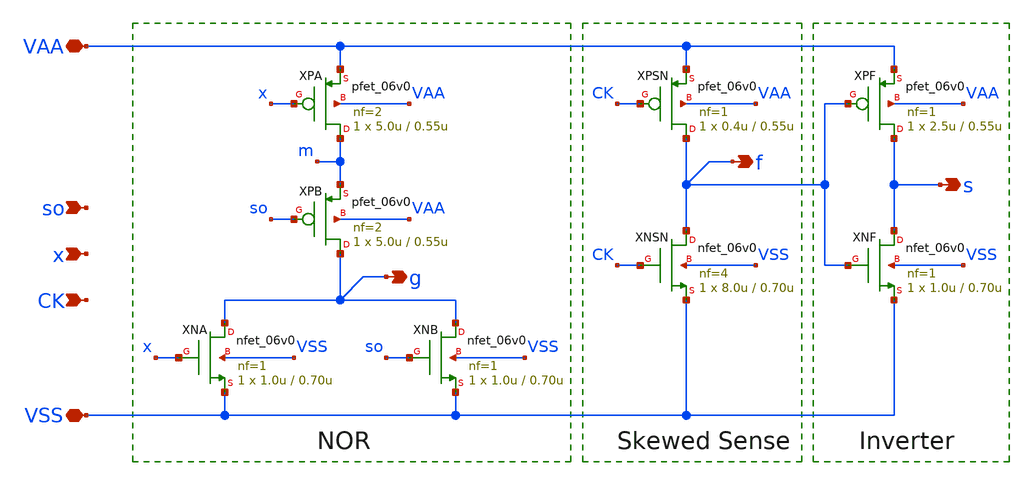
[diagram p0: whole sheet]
** sch_path: xschem/ck_a.sch
**.subckt ck_a so VAA VSS x g CK f s
*.ipin so
*.iopin VAA
*.iopin VSS
*.ipin x
*.opin g
*.ipin CK
*.opin f
*.opin s
XPA m x VAA VAA pfet_06v0 L=0.55u W=5.0u nf=2 ad='int((nf+1)/2) * W/nf * 0.18u' as='int((nf+2)/2) * W/nf * 0.18u'
+ pd='2*int((nf+1)/2) * (W/nf + 0.18u)' ps='2*int((nf+2)/2) * (W/nf + 0.18u)' nrd='0.18u / W' nrs='0.18u / W'
+ sa=0 sb=0 sd=0 m=1
XPB g so m VAA pfet_06v0 L=0.55u W=5.0u nf=2 ad='int((nf+1)/2) * W/nf * 0.18u' as='int((nf+2)/2) * W/nf * 0.18u'
+ pd='2*int((nf+1)/2) * (W/nf + 0.18u)' ps='2*int((nf+2)/2) * (W/nf + 0.18u)' nrd='0.18u / W' nrs='0.18u / W'
+ sa=0 sb=0 sd=0 m=1
XNA g x VSS VSS nfet_06v0 L=0.70u W=1.0u nf=1 ad='int((nf+1)/2) * W/nf * 0.18u' as='int((nf+2)/2) * W/nf * 0.18u'
+ pd='2*int((nf+1)/2) * (W/nf + 0.18u)' ps='2*int((nf+2)/2) * (W/nf + 0.18u)' nrd='0.18u / W' nrs='0.18u / W'
+ sa=0 sb=0 sd=0 m=1 par=1
XNB g so VSS VSS nfet_06v0 L=0.70u W=1.0u nf=1 ad='int((nf+1)/2) * W/nf * 0.18u' as='int((nf+2)/2) * W/nf * 0.18u'
+ pd='2*int((nf+1)/2) * (W/nf + 0.18u)' ps='2*int((nf+2)/2) * (W/nf + 0.18u)' nrd='0.18u / W' nrs='0.18u / W'
+ sa=0 sb=0 sd=0 m=1 par=1
XPSN f CK VAA VAA pfet_06v0 L=0.55u W=0.4u nf=1 ad='int((nf+1)/2) * W/nf * 0.18u' as='int((nf+2)/2) * W/nf * 0.18u'
+ pd='2*int((nf+1)/2) * (W/nf + 0.18u)' ps='2*int((nf+2)/2) * (W/nf + 0.18u)' nrd='0.18u / W' nrs='0.18u / W'
+ sa=0 sb=0 sd=0 m=1
XNSN f CK VSS VSS nfet_06v0 L=0.70u W=8.0u nf=4 ad='int((nf+1)/2) * W/nf * 0.18u' as='int((nf+2)/2) * W/nf * 0.18u'
+ pd='2*int((nf+1)/2) * (W/nf + 0.18u)' ps='2*int((nf+2)/2) * (W/nf + 0.18u)' nrd='0.18u / W' nrs='0.18u / W'
+ sa=0 sb=0 sd=0 m=1 par=1
XPF s f VAA VAA pfet_06v0 L=0.55u W=2.5u nf=1 ad='int((nf+1)/2) * W/nf * 0.18u' as='int((nf+2)/2) * W/nf * 0.18u'
+ pd='2*int((nf+1)/2) * (W/nf + 0.18u)' ps='2*int((nf+2)/2) * (W/nf + 0.18u)' nrd='0.18u / W' nrs='0.18u / W'
+ sa=0 sb=0 sd=0 m=1
XNF s f VSS VSS nfet_06v0 L=0.70u W=1.0u nf=1 ad='int((nf+1)/2) * W/nf * 0.18u' as='int((nf+2)/2) * W/nf * 0.18u'
+ pd='2*int((nf+1)/2) * (W/nf + 0.18u)' ps='2*int((nf+2)/2) * (W/nf + 0.18u)' nrd='0.18u / W' nrs='0.18u / W'
+ sa=0 sb=0 sd=0 m=1 par=1
**.ends
.end
